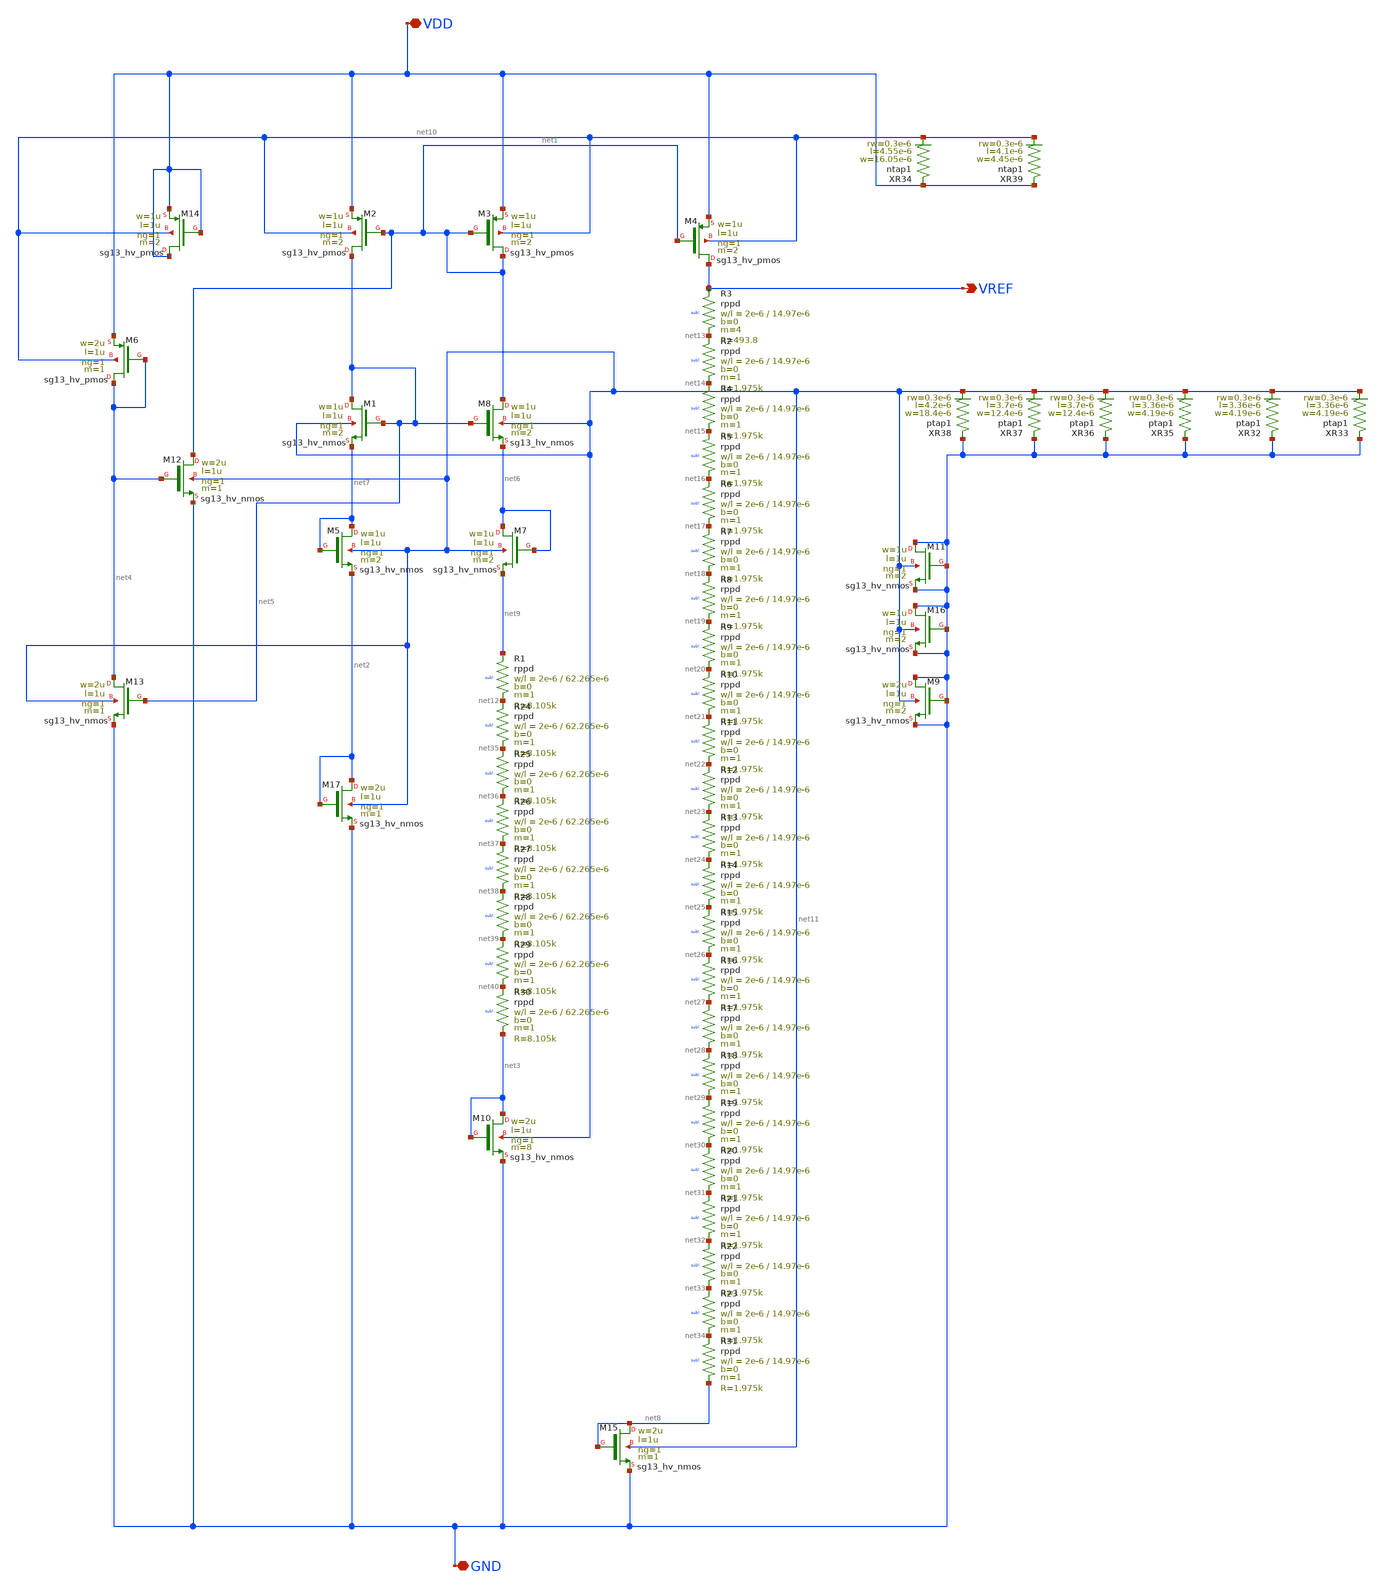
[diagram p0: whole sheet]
** sch_path: dependencies/BGR/BGR-main/netlist/schematic/BGR.sch
**.subckt BGR VDD GND VREF
*.iopin VDD
*.iopin GND
*.opin VREF
XM2 net5 net1 VDD net10 sg13_hv_pmos w=1u l=1u ng=1 m=2 mm_ok=1
XM3 net1 net1 VDD net10 sg13_hv_pmos w=1u l=1u ng=1 m=2 mm_ok=1
XM4 VREF net1 VDD net10 sg13_hv_pmos w=1u l=1u ng=1 m=2 mm_ok=1
XM9 GND GND GND net11 sg13_hv_nmos w=2u l=1u ng=1 m=2 mm_ok=1
XM10 net3 net3 GND net11 sg13_hv_nmos w=2u l=1u ng=1 m=8 mm_ok=1
XM12 net1 net4 GND net11 sg13_hv_nmos w=2u l=1u ng=1 m=1 mm_ok=1
XM13 net4 net5 GND net11 sg13_hv_nmos w=2u l=1u ng=1 m=1 mm_ok=1
XM1 net5 net5 net7 net11 sg13_hv_nmos w=1u l=1u ng=1 m=2 mm_ok=1
XM5 net7 net7 net2 net11 sg13_hv_nmos w=1u l=1u ng=1 m=2 mm_ok=1
XM7 net6 net6 net9 net11 sg13_hv_nmos w=1u l=1u ng=1 m=2 mm_ok=1
XM8 net1 net5 net6 net11 sg13_hv_nmos w=1u l=1u ng=1 m=2 mm_ok=1
XR1 net9 net12 sub! rppd w=2e-6 l=62.265e-6 m=1 b=0 mm_ok=1
XM6 net4 net4 VDD net10 sg13_hv_pmos w=2u l=1u ng=1 m=1 mm_ok=1
XR3 VREF net13 sub! rppd w=2e-6 l=14.97e-6 m=4 b=0 mm_ok=1
XR2 net13 net14 sub! rppd w=2e-6 l=14.97e-6 m=1 b=0 mm_ok=1
XR4 net14 net15 sub! rppd w=2e-6 l=14.97e-6 m=1 b=0 mm_ok=1
XR5 net15 net16 sub! rppd w=2e-6 l=14.97e-6 m=1 b=0 mm_ok=1
XR34 VDD net10 ntap1 R=5.698 w=16.05e-6 l=4.55e-6 rw=0.3e-6
XR32 GND net11 ptap1 R=16.4 w=4.19e-6 l=3.36e-6 rw=0.3e-6
XR35 GND net11 ptap1 R=16.4 w=4.19e-6 l=3.36e-6 rw=0.3e-6
XR36 GND net11 ptap1 R=7.352 w=12.4e-6 l=3.7e-6 rw=0.3e-6
XR37 GND net11 ptap1 R=7.352 w=12.4e-6 l=3.7e-6 rw=0.3e-6
XR38 GND net11 ptap1 R=5.18 w=18.4e-6 l=4.2e-6 rw=0.3e-6
XM14 VDD VDD VDD net10 sg13_hv_pmos w=1u l=1u ng=1 m=2 mm_ok=1
XR39 VDD net10 ntap1 R=14.33 w=4.45e-6 l=4.1e-6 rw=0.3e-6
XR33 GND net11 ptap1 R=16.4 w=4.19e-6 l=3.36e-6 rw=0.3e-6
XM15 net8 net8 GND net11 sg13_hv_nmos w=2u l=1u ng=1 m=1 mm_ok=1
XM11 GND GND GND net11 sg13_hv_nmos w=1u l=1u ng=1 m=2 mm_ok=1
XM16 GND GND GND net11 sg13_hv_nmos w=1u l=1u ng=1 m=2 mm_ok=1
XM17 net2 net2 GND net11 sg13_hv_nmos w=2u l=1u ng=1 m=1 mm_ok=1
XR6 net16 net17 sub! rppd w=2e-6 l=14.97e-6 m=1 b=0 mm_ok=1
XR7 net17 net18 sub! rppd w=2e-6 l=14.97e-6 m=1 b=0 mm_ok=1
XR8 net18 net19 sub! rppd w=2e-6 l=14.97e-6 m=1 b=0 mm_ok=1
XR9 net19 net20 sub! rppd w=2e-6 l=14.97e-6 m=1 b=0 mm_ok=1
XR10 net20 net21 sub! rppd w=2e-6 l=14.97e-6 m=1 b=0 mm_ok=1
XR11 net21 net22 sub! rppd w=2e-6 l=14.97e-6 m=1 b=0 mm_ok=1
XR12 net22 net23 sub! rppd w=2e-6 l=14.97e-6 m=1 b=0 mm_ok=1
XR13 net23 net24 sub! rppd w=2e-6 l=14.97e-6 m=1 b=0 mm_ok=1
XR14 net24 net25 sub! rppd w=2e-6 l=14.97e-6 m=1 b=0 mm_ok=1
XR15 net25 net26 sub! rppd w=2e-6 l=14.97e-6 m=1 b=0 mm_ok=1
XR16 net26 net27 sub! rppd w=2e-6 l=14.97e-6 m=1 b=0 mm_ok=1
XR17 net27 net28 sub! rppd w=2e-6 l=14.97e-6 m=1 b=0 mm_ok=1
XR18 net28 net29 sub! rppd w=2e-6 l=14.97e-6 m=1 b=0 mm_ok=1
XR19 net29 net30 sub! rppd w=2e-6 l=14.97e-6 m=1 b=0 mm_ok=1
XR20 net30 net31 sub! rppd w=2e-6 l=14.97e-6 m=1 b=0 mm_ok=1
XR21 net31 net32 sub! rppd w=2e-6 l=14.97e-6 m=1 b=0 mm_ok=1
XR22 net32 net33 sub! rppd w=2e-6 l=14.97e-6 m=1 b=0 mm_ok=1
XR23 net33 net34 sub! rppd w=2e-6 l=14.97e-6 m=1 b=0 mm_ok=1
XR31 net34 net8 sub! rppd w=2e-6 l=14.97e-6 m=1 b=0 mm_ok=1
XR24 net12 net35 sub! rppd w=2e-6 l=62.265e-6 m=1 b=0 mm_ok=1
XR25 net35 net36 sub! rppd w=2e-6 l=62.265e-6 m=1 b=0 mm_ok=1
XR26 net36 net37 sub! rppd w=2e-6 l=62.265e-6 m=1 b=0 mm_ok=1
XR27 net37 net38 sub! rppd w=2e-6 l=62.265e-6 m=1 b=0 mm_ok=1
XR28 net38 net39 sub! rppd w=2e-6 l=62.265e-6 m=1 b=0 mm_ok=1
XR29 net39 net40 sub! rppd w=2e-6 l=62.265e-6 m=1 b=0 mm_ok=1
XR30 net40 net3 sub! rppd w=2e-6 l=62.265e-6 m=1 b=0 mm_ok=1
**.ends
.end
